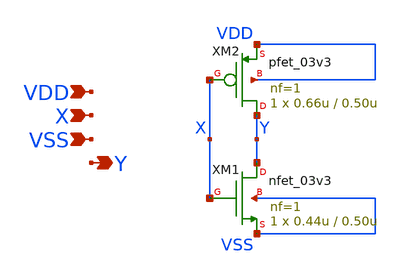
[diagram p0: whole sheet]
** sch_path: xschem/inv.sch
**.subckt inv VDD X VSS Y
*.ipin VDD
*.ipin X
*.ipin VSS
*.opin Y
XM1 Y X VSS VSS nfet_03v3 L=0.50u W=0.44u nf=1 ad='int((nf+1)/2) * W/nf * 0.18u' as='int((nf+2)/2) * W/nf * 0.18u'
+ pd='2*int((nf+1)/2) * (W/nf + 0.18u)' ps='2*int((nf+2)/2) * (W/nf + 0.18u)' nrd='0.18u / W' nrs='0.18u / W'
+ sa=0 sb=0 sd=0 m=1
XM2 Y X VDD VDD pfet_03v3 L=0.50u W=0.66u nf=1 ad='int((nf+1)/2) * W/nf * 0.18u' as='int((nf+2)/2) * W/nf * 0.18u'
+ pd='2*int((nf+1)/2) * (W/nf + 0.18u)' ps='2*int((nf+2)/2) * (W/nf + 0.18u)' nrd='0.18u / W' nrs='0.18u / W'
+ sa=0 sb=0 sd=0 m=1
**.ends
.end
